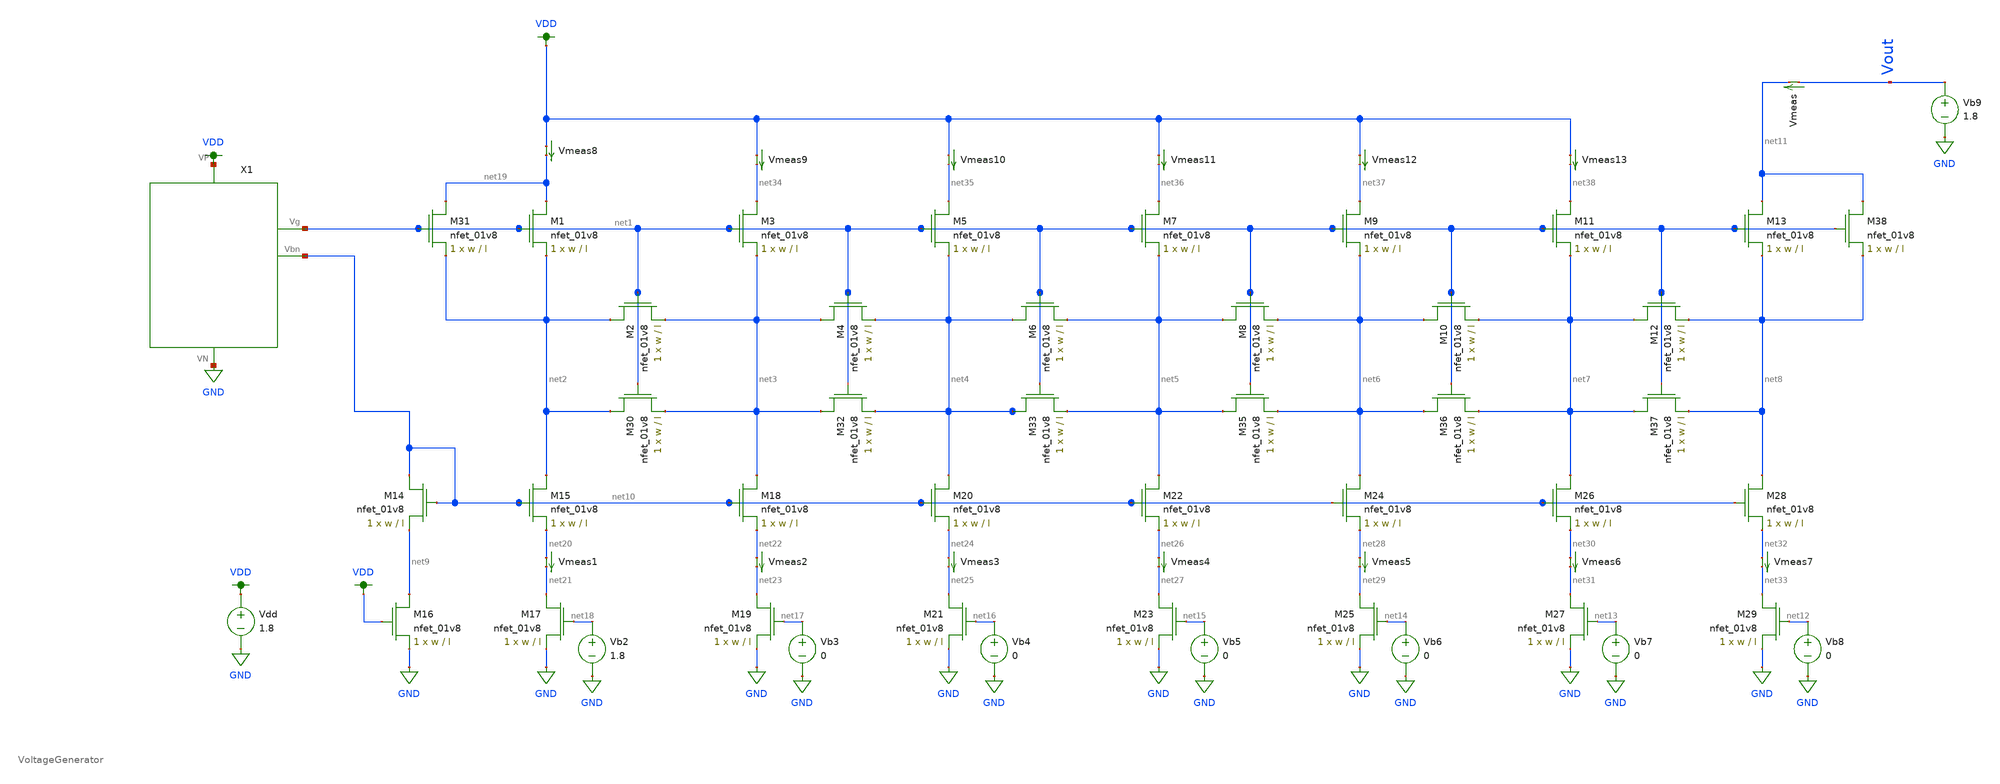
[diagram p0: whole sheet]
** sch_path: DAC_dnl_script.sch
**.subckt DAC_dnl_script
XM1 net19 net1 net2 GND sky130_fd_pr__nfet_01v8 L=l W=w nf=1 ad='int((nf+1)/2) * W/nf * 0.29' as='int((nf+2)/2) * W/nf * 0.29'
+ pd='2*int((nf+1)/2) * (W/nf + 0.29)' ps='2*int((nf+2)/2) * (W/nf + 0.29)' nrd='0.29 / W' nrs='0.29 / W'
+ sa=0 sb=0 sd=0 mult=1 m=1
XM2 net2 net1 net3 GND sky130_fd_pr__nfet_01v8 L=l W=w nf=1 ad='int((nf+1)/2) * W/nf * 0.29' as='int((nf+2)/2) * W/nf * 0.29'
+ pd='2*int((nf+1)/2) * (W/nf + 0.29)' ps='2*int((nf+2)/2) * (W/nf + 0.29)' nrd='0.29 / W' nrs='0.29 / W'
+ sa=0 sb=0 sd=0 mult=1 m=1
XM3 net34 net1 net3 GND sky130_fd_pr__nfet_01v8 L=l W=w nf=1 ad='int((nf+1)/2) * W/nf * 0.29' as='int((nf+2)/2) * W/nf * 0.29'
+ pd='2*int((nf+1)/2) * (W/nf + 0.29)' ps='2*int((nf+2)/2) * (W/nf + 0.29)' nrd='0.29 / W' nrs='0.29 / W'
+ sa=0 sb=0 sd=0 mult=1 m=1
XM4 net3 net1 net4 GND sky130_fd_pr__nfet_01v8 L=l W=w nf=1 ad='int((nf+1)/2) * W/nf * 0.29' as='int((nf+2)/2) * W/nf * 0.29'
+ pd='2*int((nf+1)/2) * (W/nf + 0.29)' ps='2*int((nf+2)/2) * (W/nf + 0.29)' nrd='0.29 / W' nrs='0.29 / W'
+ sa=0 sb=0 sd=0 mult=1 m=1
XM5 net35 net1 net4 GND sky130_fd_pr__nfet_01v8 L=l W=w nf=1 ad='int((nf+1)/2) * W/nf * 0.29' as='int((nf+2)/2) * W/nf * 0.29'
+ pd='2*int((nf+1)/2) * (W/nf + 0.29)' ps='2*int((nf+2)/2) * (W/nf + 0.29)' nrd='0.29 / W' nrs='0.29 / W'
+ sa=0 sb=0 sd=0 mult=1 m=1
XM6 net4 net1 net5 GND sky130_fd_pr__nfet_01v8 L=l W=w nf=1 ad='int((nf+1)/2) * W/nf * 0.29' as='int((nf+2)/2) * W/nf * 0.29'
+ pd='2*int((nf+1)/2) * (W/nf + 0.29)' ps='2*int((nf+2)/2) * (W/nf + 0.29)' nrd='0.29 / W' nrs='0.29 / W'
+ sa=0 sb=0 sd=0 mult=1 m=1
XM7 net36 net1 net5 GND sky130_fd_pr__nfet_01v8 L=l W=w nf=1 ad='int((nf+1)/2) * W/nf * 0.29' as='int((nf+2)/2) * W/nf * 0.29'
+ pd='2*int((nf+1)/2) * (W/nf + 0.29)' ps='2*int((nf+2)/2) * (W/nf + 0.29)' nrd='0.29 / W' nrs='0.29 / W'
+ sa=0 sb=0 sd=0 mult=1 m=1
XM8 net5 net1 net6 GND sky130_fd_pr__nfet_01v8 L=l W=w nf=1 ad='int((nf+1)/2) * W/nf * 0.29' as='int((nf+2)/2) * W/nf * 0.29'
+ pd='2*int((nf+1)/2) * (W/nf + 0.29)' ps='2*int((nf+2)/2) * (W/nf + 0.29)' nrd='0.29 / W' nrs='0.29 / W'
+ sa=0 sb=0 sd=0 mult=1 m=1
XM9 net37 net1 net6 GND sky130_fd_pr__nfet_01v8 L=l W=w nf=1 ad='int((nf+1)/2) * W/nf * 0.29' as='int((nf+2)/2) * W/nf * 0.29'
+ pd='2*int((nf+1)/2) * (W/nf + 0.29)' ps='2*int((nf+2)/2) * (W/nf + 0.29)' nrd='0.29 / W' nrs='0.29 / W'
+ sa=0 sb=0 sd=0 mult=1 m=1
XM10 net6 net1 net7 GND sky130_fd_pr__nfet_01v8 L=l W=w nf=1 ad='int((nf+1)/2) * W/nf * 0.29' as='int((nf+2)/2) * W/nf * 0.29'
+ pd='2*int((nf+1)/2) * (W/nf + 0.29)' ps='2*int((nf+2)/2) * (W/nf + 0.29)' nrd='0.29 / W' nrs='0.29 / W'
+ sa=0 sb=0 sd=0 mult=1 m=1
XM11 net38 net1 net7 GND sky130_fd_pr__nfet_01v8 L=l W=w nf=1 ad='int((nf+1)/2) * W/nf * 0.29' as='int((nf+2)/2) * W/nf * 0.29'
+ pd='2*int((nf+1)/2) * (W/nf + 0.29)' ps='2*int((nf+2)/2) * (W/nf + 0.29)' nrd='0.29 / W' nrs='0.29 / W'
+ sa=0 sb=0 sd=0 mult=1 m=1
XM12 net7 net1 net8 GND sky130_fd_pr__nfet_01v8 L=l W=w nf=1 ad='int((nf+1)/2) * W/nf * 0.29' as='int((nf+2)/2) * W/nf * 0.29'
+ pd='2*int((nf+1)/2) * (W/nf + 0.29)' ps='2*int((nf+2)/2) * (W/nf + 0.29)' nrd='0.29 / W' nrs='0.29 / W'
+ sa=0 sb=0 sd=0 mult=1 m=1
XM13 net11 net1 net8 GND sky130_fd_pr__nfet_01v8 L=l W=w nf=1 ad='int((nf+1)/2) * W/nf * 0.29' as='int((nf+2)/2) * W/nf * 0.29'
+ pd='2*int((nf+1)/2) * (W/nf + 0.29)' ps='2*int((nf+2)/2) * (W/nf + 0.29)' nrd='0.29 / W' nrs='0.29 / W'
+ sa=0 sb=0 sd=0 mult=1 m=1
XM14 net10 net10 net9 GND sky130_fd_pr__nfet_01v8 L=l W=w nf=1 ad='int((nf+1)/2) * W/nf * 0.29' as='int((nf+2)/2) * W/nf * 0.29'
+ pd='2*int((nf+1)/2) * (W/nf + 0.29)' ps='2*int((nf+2)/2) * (W/nf + 0.29)' nrd='0.29 / W' nrs='0.29 / W'
+ sa=0 sb=0 sd=0 mult=1 m=1
XM15 net2 net10 net20 GND sky130_fd_pr__nfet_01v8 L=l W=w nf=1 ad='int((nf+1)/2) * W/nf * 0.29' as='int((nf+2)/2) * W/nf * 0.29'
+ pd='2*int((nf+1)/2) * (W/nf + 0.29)' ps='2*int((nf+2)/2) * (W/nf + 0.29)' nrd='0.29 / W' nrs='0.29 / W'
+ sa=0 sb=0 sd=0 mult=1 m=1
XM16 net9 VDD GND GND sky130_fd_pr__nfet_01v8 L=l W=w nf=1 ad='int((nf+1)/2) * W/nf * 0.29' as='int((nf+2)/2) * W/nf * 0.29'
+ pd='2*int((nf+1)/2) * (W/nf + 0.29)' ps='2*int((nf+2)/2) * (W/nf + 0.29)' nrd='0.29 / W' nrs='0.29 / W'
+ sa=0 sb=0 sd=0 mult=1 m=1
XM17 net21 net18 GND GND sky130_fd_pr__nfet_01v8 L=l W=w nf=1 ad='int((nf+1)/2) * W/nf * 0.29' as='int((nf+2)/2) * W/nf * 0.29'
+ pd='2*int((nf+1)/2) * (W/nf + 0.29)' ps='2*int((nf+2)/2) * (W/nf + 0.29)' nrd='0.29 / W' nrs='0.29 / W'
+ sa=0 sb=0 sd=0 mult=1 m=1
XM18 net3 net10 net22 GND sky130_fd_pr__nfet_01v8 L=l W=w nf=1 ad='int((nf+1)/2) * W/nf * 0.29' as='int((nf+2)/2) * W/nf * 0.29'
+ pd='2*int((nf+1)/2) * (W/nf + 0.29)' ps='2*int((nf+2)/2) * (W/nf + 0.29)' nrd='0.29 / W' nrs='0.29 / W'
+ sa=0 sb=0 sd=0 mult=1 m=1
XM19 net23 net17 GND GND sky130_fd_pr__nfet_01v8 L=l W=w nf=1 ad='int((nf+1)/2) * W/nf * 0.29' as='int((nf+2)/2) * W/nf * 0.29'
+ pd='2*int((nf+1)/2) * (W/nf + 0.29)' ps='2*int((nf+2)/2) * (W/nf + 0.29)' nrd='0.29 / W' nrs='0.29 / W'
+ sa=0 sb=0 sd=0 mult=1 m=1
XM20 net4 net10 net24 GND sky130_fd_pr__nfet_01v8 L=l W=w nf=1 ad='int((nf+1)/2) * W/nf * 0.29' as='int((nf+2)/2) * W/nf * 0.29'
+ pd='2*int((nf+1)/2) * (W/nf + 0.29)' ps='2*int((nf+2)/2) * (W/nf + 0.29)' nrd='0.29 / W' nrs='0.29 / W'
+ sa=0 sb=0 sd=0 mult=1 m=1
XM21 net25 net16 GND GND sky130_fd_pr__nfet_01v8 L=l W=w nf=1 ad='int((nf+1)/2) * W/nf * 0.29' as='int((nf+2)/2) * W/nf * 0.29'
+ pd='2*int((nf+1)/2) * (W/nf + 0.29)' ps='2*int((nf+2)/2) * (W/nf + 0.29)' nrd='0.29 / W' nrs='0.29 / W'
+ sa=0 sb=0 sd=0 mult=1 m=1
XM22 net5 net10 net26 GND sky130_fd_pr__nfet_01v8 L=l W=w nf=1 ad='int((nf+1)/2) * W/nf * 0.29' as='int((nf+2)/2) * W/nf * 0.29'
+ pd='2*int((nf+1)/2) * (W/nf + 0.29)' ps='2*int((nf+2)/2) * (W/nf + 0.29)' nrd='0.29 / W' nrs='0.29 / W'
+ sa=0 sb=0 sd=0 mult=1 m=1
XM23 net27 net15 GND GND sky130_fd_pr__nfet_01v8 L=l W=w nf=1 ad='int((nf+1)/2) * W/nf * 0.29' as='int((nf+2)/2) * W/nf * 0.29'
+ pd='2*int((nf+1)/2) * (W/nf + 0.29)' ps='2*int((nf+2)/2) * (W/nf + 0.29)' nrd='0.29 / W' nrs='0.29 / W'
+ sa=0 sb=0 sd=0 mult=1 m=1
XM24 net6 net10 net28 GND sky130_fd_pr__nfet_01v8 L=l W=w nf=1 ad='int((nf+1)/2) * W/nf * 0.29' as='int((nf+2)/2) * W/nf * 0.29'
+ pd='2*int((nf+1)/2) * (W/nf + 0.29)' ps='2*int((nf+2)/2) * (W/nf + 0.29)' nrd='0.29 / W' nrs='0.29 / W'
+ sa=0 sb=0 sd=0 mult=1 m=1
XM25 net29 net14 GND GND sky130_fd_pr__nfet_01v8 L=l W=w nf=1 ad='int((nf+1)/2) * W/nf * 0.29' as='int((nf+2)/2) * W/nf * 0.29'
+ pd='2*int((nf+1)/2) * (W/nf + 0.29)' ps='2*int((nf+2)/2) * (W/nf + 0.29)' nrd='0.29 / W' nrs='0.29 / W'
+ sa=0 sb=0 sd=0 mult=1 m=1
XM26 net7 net10 net30 GND sky130_fd_pr__nfet_01v8 L=l W=w nf=1 ad='int((nf+1)/2) * W/nf * 0.29' as='int((nf+2)/2) * W/nf * 0.29'
+ pd='2*int((nf+1)/2) * (W/nf + 0.29)' ps='2*int((nf+2)/2) * (W/nf + 0.29)' nrd='0.29 / W' nrs='0.29 / W'
+ sa=0 sb=0 sd=0 mult=1 m=1
XM27 net31 net13 GND GND sky130_fd_pr__nfet_01v8 L=l W=w nf=1 ad='int((nf+1)/2) * W/nf * 0.29' as='int((nf+2)/2) * W/nf * 0.29'
+ pd='2*int((nf+1)/2) * (W/nf + 0.29)' ps='2*int((nf+2)/2) * (W/nf + 0.29)' nrd='0.29 / W' nrs='0.29 / W'
+ sa=0 sb=0 sd=0 mult=1 m=1
XM28 net8 net10 net32 GND sky130_fd_pr__nfet_01v8 L=l W=w nf=1 ad='int((nf+1)/2) * W/nf * 0.29' as='int((nf+2)/2) * W/nf * 0.29'
+ pd='2*int((nf+1)/2) * (W/nf + 0.29)' ps='2*int((nf+2)/2) * (W/nf + 0.29)' nrd='0.29 / W' nrs='0.29 / W'
+ sa=0 sb=0 sd=0 mult=1 m=1
XM29 net33 net12 GND GND sky130_fd_pr__nfet_01v8 L=l W=w nf=1 ad='int((nf+1)/2) * W/nf * 0.29' as='int((nf+2)/2) * W/nf * 0.29'
+ pd='2*int((nf+1)/2) * (W/nf + 0.29)' ps='2*int((nf+2)/2) * (W/nf + 0.29)' nrd='0.29 / W' nrs='0.29 / W'
+ sa=0 sb=0 sd=0 mult=1 m=1
XM30 net2 net1 net3 GND sky130_fd_pr__nfet_01v8 L=l W=w nf=1 ad='int((nf+1)/2) * W/nf * 0.29' as='int((nf+2)/2) * W/nf * 0.29'
+ pd='2*int((nf+1)/2) * (W/nf + 0.29)' ps='2*int((nf+2)/2) * (W/nf + 0.29)' nrd='0.29 / W' nrs='0.29 / W'
+ sa=0 sb=0 sd=0 mult=1 m=1
XM31 net19 net1 net2 GND sky130_fd_pr__nfet_01v8 L=l W=w nf=1 ad='int((nf+1)/2) * W/nf * 0.29' as='int((nf+2)/2) * W/nf * 0.29'
+ pd='2*int((nf+1)/2) * (W/nf + 0.29)' ps='2*int((nf+2)/2) * (W/nf + 0.29)' nrd='0.29 / W' nrs='0.29 / W'
+ sa=0 sb=0 sd=0 mult=1 m=1
XM32 net3 net1 net4 GND sky130_fd_pr__nfet_01v8 L=l W=w nf=1 ad='int((nf+1)/2) * W/nf * 0.29' as='int((nf+2)/2) * W/nf * 0.29'
+ pd='2*int((nf+1)/2) * (W/nf + 0.29)' ps='2*int((nf+2)/2) * (W/nf + 0.29)' nrd='0.29 / W' nrs='0.29 / W'
+ sa=0 sb=0 sd=0 mult=1 m=1
XM33 net4 net1 net5 GND sky130_fd_pr__nfet_01v8 L=l W=w nf=1 ad='int((nf+1)/2) * W/nf * 0.29' as='int((nf+2)/2) * W/nf * 0.29'
+ pd='2*int((nf+1)/2) * (W/nf + 0.29)' ps='2*int((nf+2)/2) * (W/nf + 0.29)' nrd='0.29 / W' nrs='0.29 / W'
+ sa=0 sb=0 sd=0 mult=1 m=1
XM35 net5 net1 net6 GND sky130_fd_pr__nfet_01v8 L=l W=w nf=1 ad='int((nf+1)/2) * W/nf * 0.29' as='int((nf+2)/2) * W/nf * 0.29'
+ pd='2*int((nf+1)/2) * (W/nf + 0.29)' ps='2*int((nf+2)/2) * (W/nf + 0.29)' nrd='0.29 / W' nrs='0.29 / W'
+ sa=0 sb=0 sd=0 mult=1 m=1
XM36 net6 net1 net7 GND sky130_fd_pr__nfet_01v8 L=l W=w nf=1 ad='int((nf+1)/2) * W/nf * 0.29' as='int((nf+2)/2) * W/nf * 0.29'
+ pd='2*int((nf+1)/2) * (W/nf + 0.29)' ps='2*int((nf+2)/2) * (W/nf + 0.29)' nrd='0.29 / W' nrs='0.29 / W'
+ sa=0 sb=0 sd=0 mult=1 m=1
XM37 net7 net1 net8 GND sky130_fd_pr__nfet_01v8 L=l W=w nf=1 ad='int((nf+1)/2) * W/nf * 0.29' as='int((nf+2)/2) * W/nf * 0.29'
+ pd='2*int((nf+1)/2) * (W/nf + 0.29)' ps='2*int((nf+2)/2) * (W/nf + 0.29)' nrd='0.29 / W' nrs='0.29 / W'
+ sa=0 sb=0 sd=0 mult=1 m=1
XM38 net11 net1 net8 GND sky130_fd_pr__nfet_01v8 L=l W=w nf=1 ad='int((nf+1)/2) * W/nf * 0.29' as='int((nf+2)/2) * W/nf * 0.29'
+ pd='2*int((nf+1)/2) * (W/nf + 0.29)' ps='2*int((nf+2)/2) * (W/nf + 0.29)' nrd='0.29 / W' nrs='0.29 / W'
+ sa=0 sb=0 sd=0 mult=1 m=1
X1 GND VDD net1 net10 VoltageGenerator
Vmeas Vout net11 0
.save i(vmeas)
Vb2 net18 GND 1.8
Vb3 net17 GND 0
Vb4 net16 GND 0
Vb5 net15 GND 0
Vb6 net14 GND 0
Vb7 net13 GND 0
Vb8 net12 GND 0
Vdd VDD GND 1.8
Vb9 Vout GND 1.8
Vmeas1 net20 net21 0
.save i(vmeas1)
Vmeas2 net22 net23 0
.save i(vmeas2)
Vmeas3 net24 net25 0
.save i(vmeas3)
Vmeas4 net26 net27 0
.save i(vmeas4)
Vmeas5 net28 net29 0
.save i(vmeas5)
Vmeas6 net30 net31 0
.save i(vmeas6)
Vmeas7 net32 net33 0
.save i(vmeas7)
Vmeas8 VDD net19 0
.save i(vmeas8)
Vmeas9 VDD net34 0
.save i(vmeas9)
Vmeas10 VDD net35 0
.save i(vmeas10)
Vmeas11 VDD net36 0
.save i(vmeas11)
Vmeas12 VDD net37 0
.save i(vmeas12)
Vmeas13 VDD net38 0
.save i(vmeas13)
**** begin user architecture code

.control
set wr_singlescale
let runs = 10
let run = 1
while run <= runs
    set appendwrite = FALSE
    wr_vecnames
    let code = 0
    while code < 128
        if code eq 0
            let b0 = 0
        else
            let b0 = code % 2
        end
        if floor(code / 2) eq 0
            let b1 = 0
        else
            let b1 = floor(code / 2) % 2
        end
        if floor(code / 4) eq 0
            let b2 = 0
        else
            let b2 = floor(code / 4) % 2
        end
        if floor(code / 8) eq 0
            let b3 = 0
        else
            let b3 = floor(code / 8) % 2
        end
        if floor(code / 16) eq 0
            let b4 = 0
        else
            let b4 = floor(code / 16) % 2
        end
        if floor(code / 32) eq 0
            let b5 = 0
        else
            let b5 = floor(code / 32) % 2
        end
        if floor(code / 64) eq 0
            let b6 = 0
        else
            let b6 = floor(code / 64) % 2
        end
        alter vb0 $&b0
        alter vb1 $&b1
        alter vb2 $&b2
        alter vb3 $&b3
        alter vb4 $&b4
        alter vb5 $&b5
        alter vb6 $&b6
        save all
        op
        wrdata ~/Documents/dnl/dnl{$&run}.txt v(b0) v(b1) v(b2) v(b3) v(b4) v(b5) v(b6) i(Vmeas) v(Vout)
        if code eq 0
            set appendwrite
            set wr_vecnames = FALSE
        end
        let code = code + 1
    end
    reset
    let run = run + 1
end
quit
.endc

**** end user architecture code
**.ends
.GLOBAL GND
.GLOBAL VDD
.end
